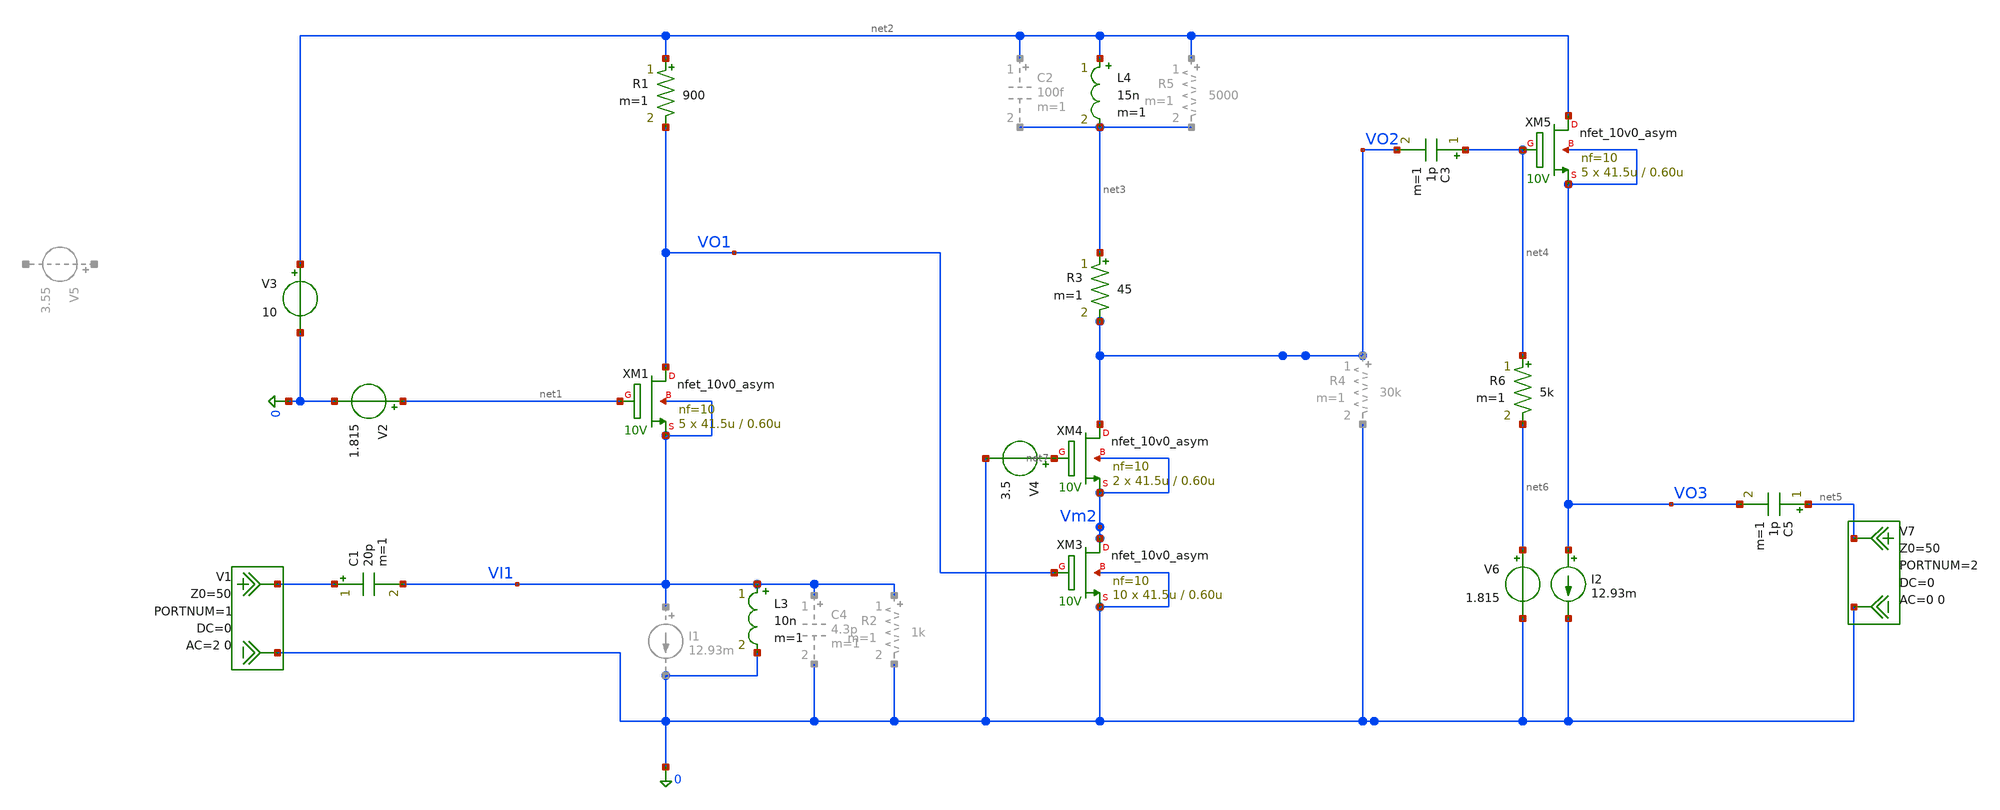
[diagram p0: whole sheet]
** sch_path: 10V0-CG/10V0-CG-STG1.sch
**.subckt 10V0-CG-STG1
XM1 VO1 net1 VI1 VI1 nfet_10v0_asym L=0.60u W=41.5u nf=10 ad='W * 1.48u' as='W * 0.48u' pd='2 * (W + 1.48u)'
+ ps='2 * (W + 0.48u)' nrd=0 nrs=0 sa=0 sb=0 sd=0 m=5
V1 VI1 0 DC 0 AC 2 0 portnum 1 z0 50
V2 net1 0 1.815
V3 net2 0 10
R1 net2 VO1 900 m=1
V7 net5 0 DC 0 AC 0 0 portnum 2 z0 50
L3 VI1 0 10n m=1
XM3 Vm2 VO1 0 0 nfet_10v0_asym L=0.60u W=41.5u nf=10 ad='W * 1.48u' as='W * 0.48u' pd='2 * (W + 1.48u)'
+ ps='2 * (W + 0.48u)' nrd=0 nrs=0 sa=0 sb=0 sd=0 m=10
XM4 VO2 net7 Vm2 Vm2 nfet_10v0_asym L=0.60u W=41.5u nf=10 ad='W * 1.48u' as='W * 0.48u' pd='2 * (W + 1.48u)'
+ ps='2 * (W + 0.48u)' nrd=0 nrs=0 sa=0 sb=0 sd=0 m=2
L4 net2 net3 15n m=1
R3 net3 VO2 45 m=1
V4 net7 0 3.5
XM5 net2 net4 VO3 VO3 nfet_10v0_asym L=0.60u W=41.5u nf=10 ad='W * 1.48u' as='W * 0.48u' pd='2 * (W + 1.48u)'
+ ps='2 * (W + 0.48u)' nrd=0 nrs=0 sa=0 sb=0 sd=0 m=5
C3 net4 VO2 1p m=1
I2 VO3 0 12.93m
V6 net6 0 1.815
R6 net4 net6 5k m=1
C5 net5 VO3 1p m=1
**** begin user architecture code

.include $::180MCU_MODELS/design.ngspice
.lib $::180MCU_MODELS/sm141064.ngspice typical
.lib $::180MCU_MODELS/smbb000149.ngspice typical



.control
op

save all
save @m.xm1.m0[gm] @m.xm1.m0[id] @m.xm1.m0[gds] @m.xm1.m0[vth] @m.xm1.m0[vdsat]
save @m.xm3.m0[gm] @m.xm3.m0[id] @m.xm3.m0[gds] @m.xm3.m0[vth] @m.xm3.m0[vdsat]
save @m.xm4.m0[gm] @m.xm4.m0[id] @m.xm4.m0[gds] @m.xm4.m0[vth] @m.xm4.m0[vdsat]
save @m.xm5.m0[gm] @m.xm5.m0[id] @m.xm5.m0[gds] @m.xm5.m0[vth] @m.xm5.m0[vdsat]
print @m.xm1.xm0.m0[gm] @m.xm1.xm0.m0[id]
print @m.xm3.xm0.m0[gm] @m.xm3.xm0.m0[id]
print @m.xm4.xm0.m0[gm] @m.xm4.xm0.m0[id]
print @m.xm5.xm0.m0[gm] @m.xm5.xm0.m0[id]
write 10V0-CG-STG1.raw

sp lin 1001 1 10e9 1
write 10V0-CG-STG1-sp.raw

ac lin 1001 1 10e9
write 10V0-CG-STG1-ac.raw
.endc


**** end user architecture code
**.ends
.end
